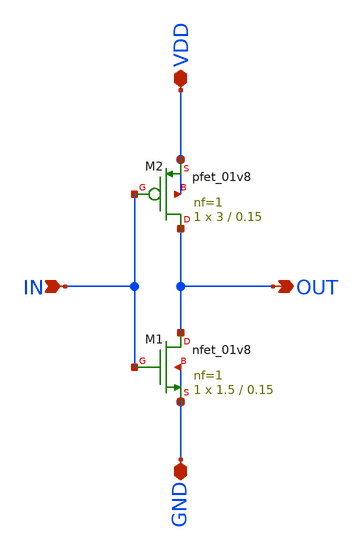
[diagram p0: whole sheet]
** sch_path: xschem/inv.sch
**.subckt inv IN OUT VDD GND
*.ipin IN
*.opin OUT
*.iopin VDD
*.iopin GND
XM1 OUT IN GND GND sky130_fd_pr__nfet_01v8 L=0.15 W=1.5 nf=1 ad='int((nf+1)/2) * W/nf * 0.29' as='int((nf+2)/2) * W/nf * 0.29'
+ pd='2*int((nf+1)/2) * (W/nf + 0.29)' ps='2*int((nf+2)/2) * (W/nf + 0.29)' nrd='0.29 / W' nrs='0.29 / W'
+ sa=0 sb=0 sd=0 mult=1 m=1
XM2 OUT IN VDD VDD sky130_fd_pr__pfet_01v8 L=0.15 W=3 nf=1 ad='int((nf+1)/2) * W/nf * 0.29' as='int((nf+2)/2) * W/nf * 0.29'
+ pd='2*int((nf+1)/2) * (W/nf + 0.29)' ps='2*int((nf+2)/2) * (W/nf + 0.29)' nrd='0.29 / W' nrs='0.29 / W'
+ sa=0 sb=0 sd=0 mult=1 m=1
**.ends
.end
